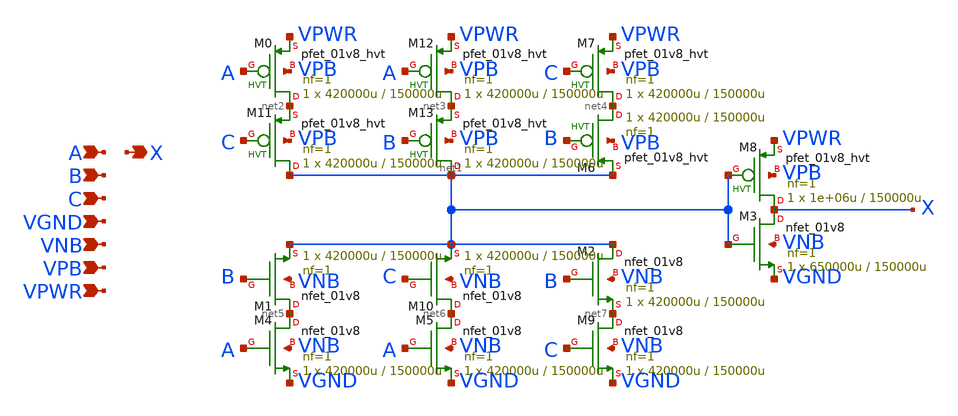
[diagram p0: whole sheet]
** sch_path: schematics/maj3/sky130_fd_sc_hd__maj3_1.sch
**.subckt sky130_fd_sc_hd__maj3_1 A B C VGND VNB VPB VPWR X
*.ipin A
*.ipin B
*.ipin C
*.ipin VGND
*.ipin VNB
*.ipin VPB
*.ipin VPWR
*.opin X
XM8 X net1 VPWR VPB sky130_fd_pr__pfet_01v8_hvt L=150000u W=1e+06u nf=1 ad='int((1 + 1)/2) * 1e+06u / 1 * 0.29'
+ as='int((1 + 2)/2) * 1e+06u / 1 * 0.29' pd='2*int((1 + 1)/2) * (1e+06u / 1 + 0.29)' ps='2*int((1 + 2)/2) * (1e+06u / 1 + 0.29)'
+ nrd='0.29 / 1e+06u ' nrs='0.29 / 1e+06u ' sa=0 sb=0 sd=0 mult=1 m=1
XM3 X net1 VGND VNB sky130_fd_pr__nfet_01v8 L=150000u W=650000u nf=1 ad='int((1 + 1)/2) * 650000u / 1 * 0.29'
+ as='int((1 + 2)/2) * 650000u / 1 * 0.29' pd='2*int((1 + 1)/2) * (650000u / 1 + 0.29)' ps='2*int((1 + 2)/2) * (650000u / 1 + 0.29)'
+ nrd='0.29 / 650000u ' nrs='0.29 / 650000u ' sa=0 sb=0 sd=0 mult=1 m=1
XM0 net2 A VPWR VPB sky130_fd_pr__pfet_01v8_hvt L=150000u W=420000u nf=1 ad='int((1 + 1)/2) * 420000u / 1 * 0.29'
+ as='int((1 + 2)/2) * 420000u / 1 * 0.29' pd='2*int((1 + 1)/2) * (420000u / 1 + 0.29)' ps='2*int((1 + 2)/2) * (420000u / 1 + 0.29)'
+ nrd='0.29 / 420000u ' nrs='0.29 / 420000u ' sa=0 sb=0 sd=0 mult=1 m=1
XM12 net3 A VPWR VPB sky130_fd_pr__pfet_01v8_hvt L=150000u W=420000u nf=1 ad='int((1 + 1)/2) * 420000u / 1 * 0.29'
+ as='int((1 + 2)/2) * 420000u / 1 * 0.29' pd='2*int((1 + 1)/2) * (420000u / 1 + 0.29)' ps='2*int((1 + 2)/2) * (420000u / 1 + 0.29)'
+ nrd='0.29 / 420000u ' nrs='0.29 / 420000u ' sa=0 sb=0 sd=0 mult=1 m=1
XM6 net4 B net1 VPB sky130_fd_pr__pfet_01v8_hvt L=150000u W=420000u nf=1 ad='int((1 + 1)/2) * 420000u / 1 * 0.29'
+ as='int((1 + 2)/2) * 420000u / 1 * 0.29' pd='2*int((1 + 1)/2) * (420000u / 1 + 0.29)' ps='2*int((1 + 2)/2) * (420000u / 1 + 0.29)'
+ nrd='0.29 / 420000u ' nrs='0.29 / 420000u ' sa=0 sb=0 sd=0 mult=1 m=1
XM13 net1 B net3 VPB sky130_fd_pr__pfet_01v8_hvt L=150000u W=420000u nf=1 ad='int((1 + 1)/2) * 420000u / 1 * 0.29'
+ as='int((1 + 2)/2) * 420000u / 1 * 0.29' pd='2*int((1 + 1)/2) * (420000u / 1 + 0.29)' ps='2*int((1 + 2)/2) * (420000u / 1 + 0.29)'
+ nrd='0.29 / 420000u ' nrs='0.29 / 420000u ' sa=0 sb=0 sd=0 mult=1 m=1
XM7 net4 C VPWR VPB sky130_fd_pr__pfet_01v8_hvt L=150000u W=420000u nf=1 ad='int((1 + 1)/2) * 420000u / 1 * 0.29'
+ as='int((1 + 2)/2) * 420000u / 1 * 0.29' pd='2*int((1 + 1)/2) * (420000u / 1 + 0.29)' ps='2*int((1 + 2)/2) * (420000u / 1 + 0.29)'
+ nrd='0.29 / 420000u ' nrs='0.29 / 420000u ' sa=0 sb=0 sd=0 mult=1 m=1
XM11 net1 C net2 VPB sky130_fd_pr__pfet_01v8_hvt L=150000u W=420000u nf=1 ad='int((1 + 1)/2) * 420000u / 1 * 0.29'
+ as='int((1 + 2)/2) * 420000u / 1 * 0.29' pd='2*int((1 + 1)/2) * (420000u / 1 + 0.29)' ps='2*int((1 + 2)/2) * (420000u / 1 + 0.29)'
+ nrd='0.29 / 420000u ' nrs='0.29 / 420000u ' sa=0 sb=0 sd=0 mult=1 m=1
XM4 net5 A VGND VNB sky130_fd_pr__nfet_01v8 L=150000u W=420000u nf=1 ad='int((1 + 1)/2) * 420000u / 1 * 0.29'
+ as='int((1 + 2)/2) * 420000u / 1 * 0.29' pd='2*int((1 + 1)/2) * (420000u / 1 + 0.29)' ps='2*int((1 + 2)/2) * (420000u / 1 + 0.29)'
+ nrd='0.29 / 420000u ' nrs='0.29 / 420000u ' sa=0 sb=0 sd=0 mult=1 m=1
XM5 net6 A VGND VNB sky130_fd_pr__nfet_01v8 L=150000u W=420000u nf=1 ad='int((1 + 1)/2) * 420000u / 1 * 0.29'
+ as='int((1 + 2)/2) * 420000u / 1 * 0.29' pd='2*int((1 + 1)/2) * (420000u / 1 + 0.29)' ps='2*int((1 + 2)/2) * (420000u / 1 + 0.29)'
+ nrd='0.29 / 420000u ' nrs='0.29 / 420000u ' sa=0 sb=0 sd=0 mult=1 m=1
XM1 net5 B net1 VNB sky130_fd_pr__nfet_01v8 L=150000u W=420000u nf=1 ad='int((1 + 1)/2) * 420000u / 1 * 0.29'
+ as='int((1 + 2)/2) * 420000u / 1 * 0.29' pd='2*int((1 + 1)/2) * (420000u / 1 + 0.29)' ps='2*int((1 + 2)/2) * (420000u / 1 + 0.29)'
+ nrd='0.29 / 420000u ' nrs='0.29 / 420000u ' sa=0 sb=0 sd=0 mult=1 m=1
XM2 net1 B net7 VNB sky130_fd_pr__nfet_01v8 L=150000u W=420000u nf=1 ad='int((1 + 1)/2) * 420000u / 1 * 0.29'
+ as='int((1 + 2)/2) * 420000u / 1 * 0.29' pd='2*int((1 + 1)/2) * (420000u / 1 + 0.29)' ps='2*int((1 + 2)/2) * (420000u / 1 + 0.29)'
+ nrd='0.29 / 420000u ' nrs='0.29 / 420000u ' sa=0 sb=0 sd=0 mult=1 m=1
XM9 net7 C VGND VNB sky130_fd_pr__nfet_01v8 L=150000u W=420000u nf=1 ad='int((1 + 1)/2) * 420000u / 1 * 0.29'
+ as='int((1 + 2)/2) * 420000u / 1 * 0.29' pd='2*int((1 + 1)/2) * (420000u / 1 + 0.29)' ps='2*int((1 + 2)/2) * (420000u / 1 + 0.29)'
+ nrd='0.29 / 420000u ' nrs='0.29 / 420000u ' sa=0 sb=0 sd=0 mult=1 m=1
XM10 net6 C net1 VNB sky130_fd_pr__nfet_01v8 L=150000u W=420000u nf=1 ad='int((1 + 1)/2) * 420000u / 1 * 0.29'
+ as='int((1 + 2)/2) * 420000u / 1 * 0.29' pd='2*int((1 + 1)/2) * (420000u / 1 + 0.29)' ps='2*int((1 + 2)/2) * (420000u / 1 + 0.29)'
+ nrd='0.29 / 420000u ' nrs='0.29 / 420000u ' sa=0 sb=0 sd=0 mult=1 m=1
**.ends
.end
